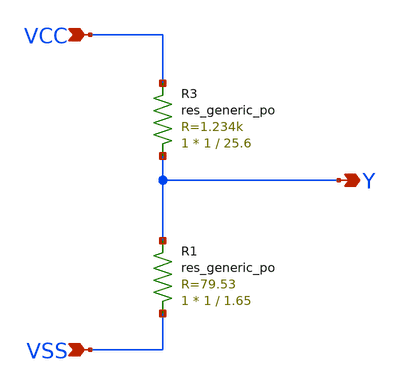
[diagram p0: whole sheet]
** sch_path: xschem/test/xschem/vDivider_02.sch
**.subckt vDivider_02 VCC VSS Y
*.ipin VCC
*.ipin VSS
*.opin Y
XR3 Y VCC sky130_fd_pr__res_generic_po W=1 L=25.6 m=1
XR1 VSS Y sky130_fd_pr__res_generic_po W=1 L=1.65 m=1
**.ends
.end
